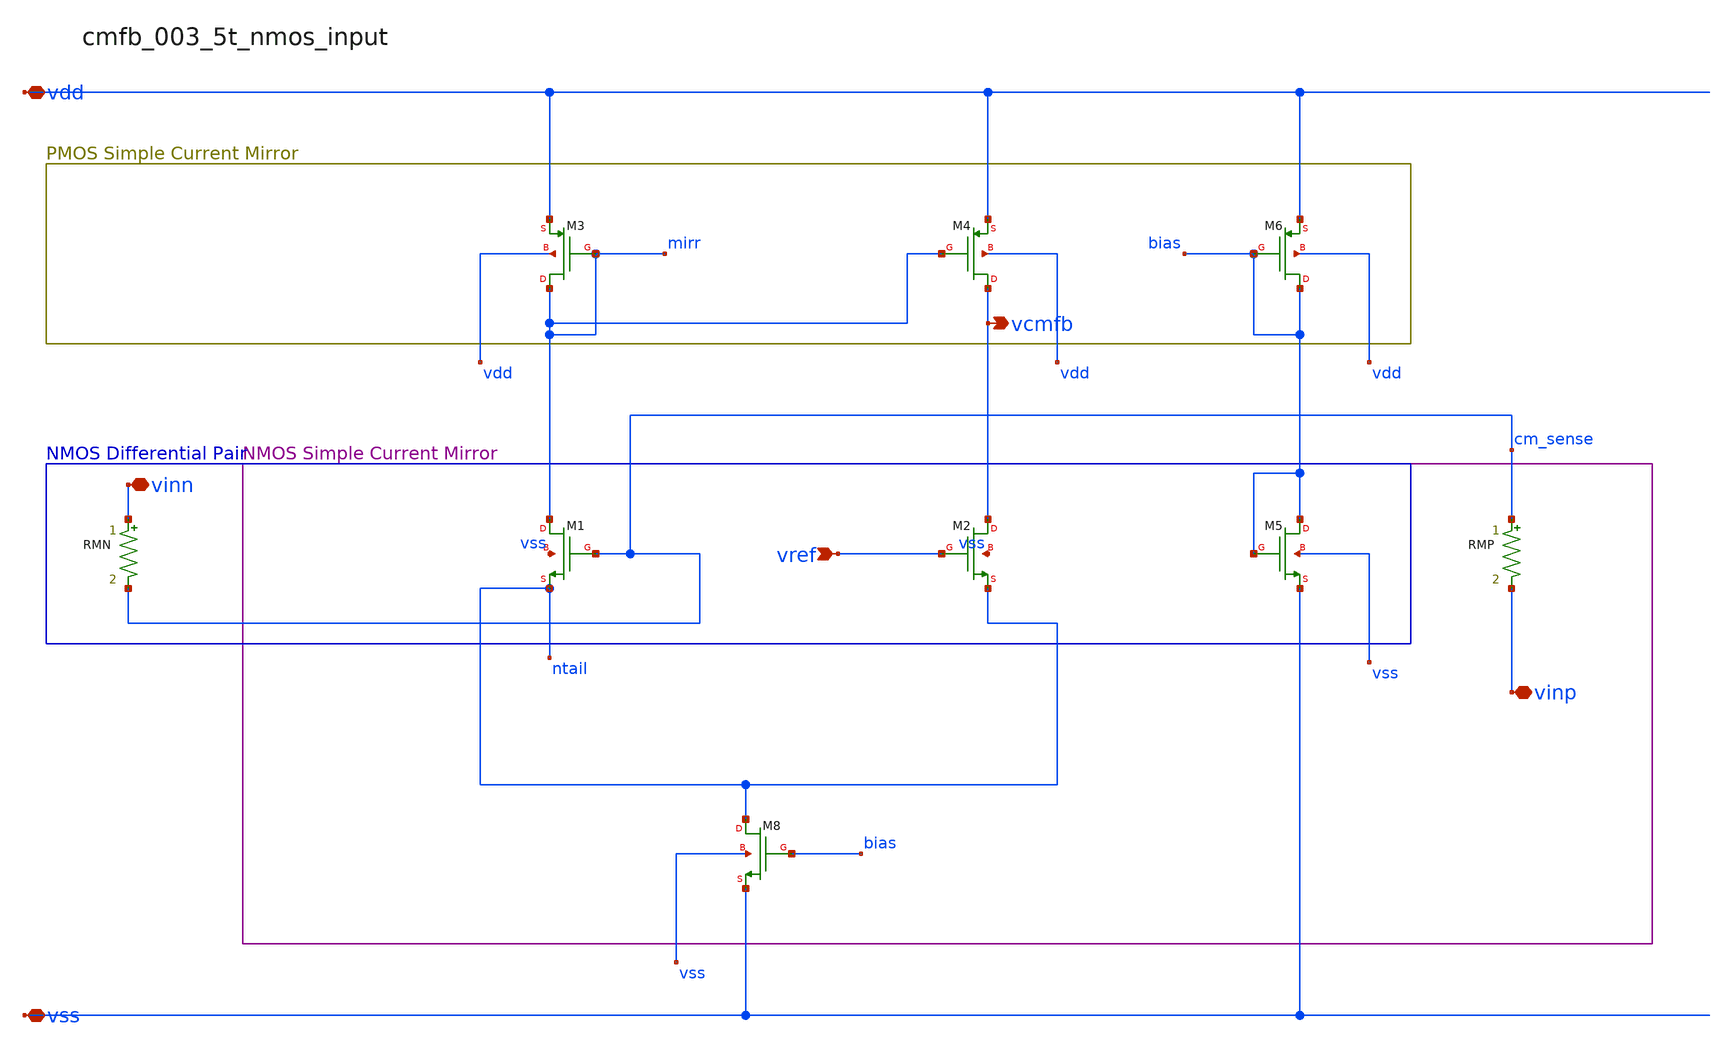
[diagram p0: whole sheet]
** sch_path: analog-db/raw/cmfb_003_5t_nmos_input/cmfb_003_5t_nmos_input_annotated.sch
**.subckt cmfb_003_5t_nmos_input_annotated vref vdd vinn vss vinp vcmfb
*.ipin vref
*.iopin vdd
*.iopin vinn
*.iopin vss
*.iopin vinp
*.opin vcmfb
RMN vinn cm_sense 'x_dut_rmn_value' m=1
RMP cm_sense vinp 'x_dut_rmp_value' m=1
XM1 mirr cm_sense ntail vss sg13_lv_nmos w=x_dut_xm1_w l=x_dut_xm1_l ng=1 m=x_dut_xm1_m
XM2 vcmfb vref ntail vss sg13_lv_nmos w=x_dut_xm2_w l=x_dut_xm2_l ng=1 m=x_dut_xm2_m
XM3 mirr mirr vdd vdd sg13_lv_pmos w=x_dut_xm3_w l=x_dut_xm3_l ng=1 m=x_dut_xm3_m
XM4 vcmfb mirr vdd vdd sg13_lv_pmos w=x_dut_xm4_w l=x_dut_xm4_l ng=1 m=x_dut_xm4_m
XM5 bias bias vss vss sg13_lv_nmos w=x_dut_xm5_w l=x_dut_xm5_l ng=1 m=x_dut_xm5_m
XM6 bias bias vdd vdd sg13_lv_pmos w=x_dut_xm6_w l=x_dut_xm6_l ng=1 m=x_dut_xm6_m
XM8 ntail bias vss vss sg13_lv_nmos w=x_dut_xm8_w l=x_dut_xm8_l ng=1 m=x_dut_xm8_m
**.ends
.end
